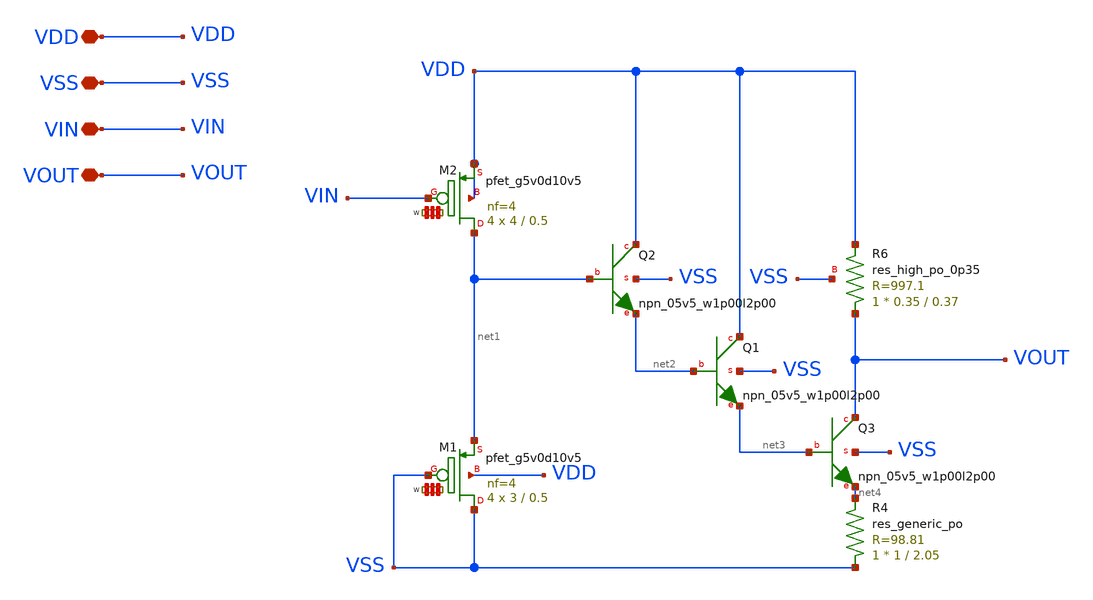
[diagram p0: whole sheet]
** sch_path: my_ip/LIB/primordial_bicmos/audio002_5V_sky130A.sch
**.subckt audio002_5V_sky130A VDD VSS VIN VOUT
*.iopin VDD
*.iopin VSS
*.iopin VIN
*.iopin VOUT
XQ2 VDD net1 net2 VSS sky130_fd_pr__npn_05v5_w1p00l2p00
XQ1 VDD net2 net3 VSS sky130_fd_pr__npn_05v5_w1p00l2p00
XQ3 VOUT net3 net4 VSS sky130_fd_pr__npn_05v5_w1p00l2p00
XM2 net1 VIN VDD VDD sky130_fd_pr__pfet_g5v0d10v5 L=0.5 W='4 * 4 ' nf=4 ad='int((4 + 1)/2) * 4 * 0.29'
+ as='int((4 + 2)/2) * 4 * 0.29' pd='2*int((4 + 1)/2) * (4 + 0.29)' ps='2*int((4 + 2)/2) * (4 + 0.29)'
+ nrd='0.29 / 4 / 4 ' nrs='0.29 / 4 / 4 ' sa=0 sb=0 sd=0 mult=4 m=4
XM1 VSS VSS net1 VDD sky130_fd_pr__pfet_g5v0d10v5 L=0.5 W='3 * 4 ' nf=4 ad='int((4 + 1)/2) * 3 * 0.29'
+ as='int((4 + 2)/2) * 3 * 0.29' pd='2*int((4 + 1)/2) * (3 + 0.29)' ps='2*int((4 + 2)/2) * (3 + 0.29)'
+ nrd='0.29 / 3 / 4 ' nrs='0.29 / 3 / 4 ' sa=0 sb=0 sd=0 mult=4 m=4
XR6 VOUT VDD VSS sky130_fd_pr__res_high_po_0p35 L=0.37 mult=1 m=1
XR4 VSS net4 sky130_fd_pr__res_generic_po W=1 L=2.05 m=1
**.ends
.end
